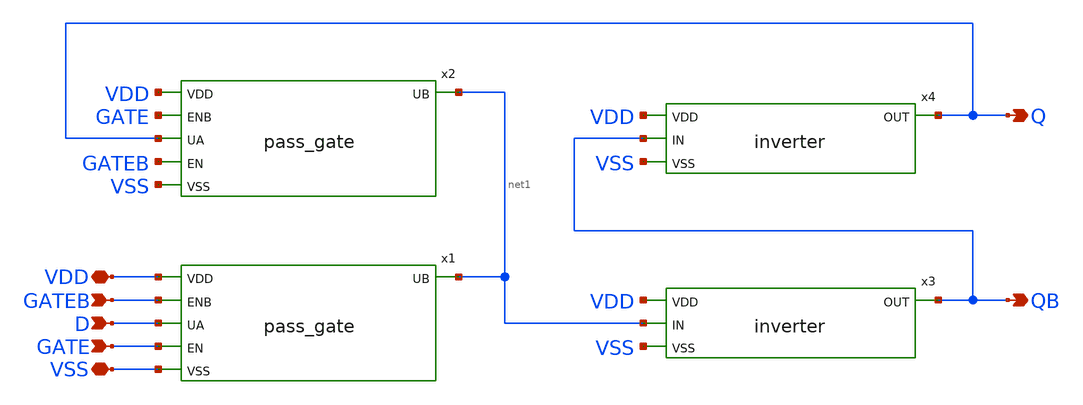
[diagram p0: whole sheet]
** sch_path: xschem/latch.sch
**.subckt latch VSS VDD D GATE GATEB Q QB
*.iopin VSS
*.iopin VDD
*.ipin D
*.ipin GATE
*.ipin GATEB
*.opin Q
*.opin QB
x1 VDD GATEB D net1 GATE VSS pass_gate
x2 VDD GATE Q net1 GATEB VSS pass_gate
x3 VDD net1 QB VSS inverter
x4 VDD QB Q VSS inverter
**.ends
.end
